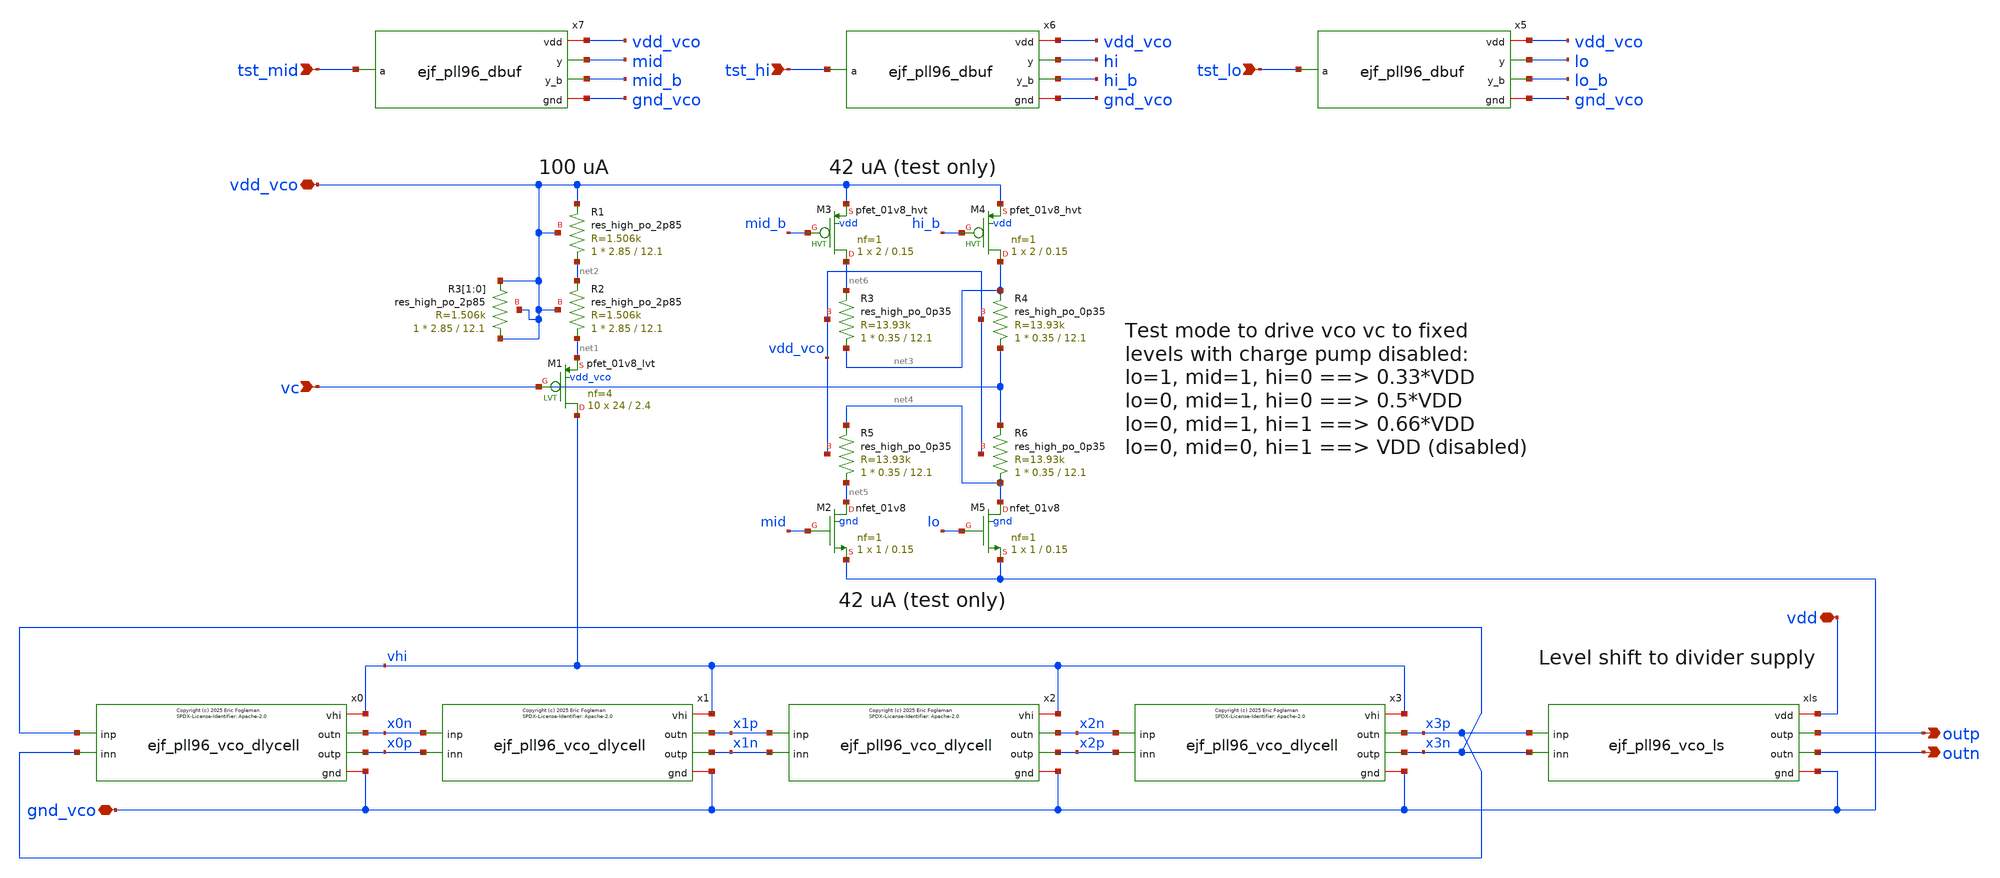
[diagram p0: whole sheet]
** sch_path: xschem/ejf_pll96_vco.sch
* xschem/ejf_pll96_vco_dlycell.sym:
* Copyright (c) 2025 Eric Fogleman
**.subckt ejf_pll96_vco vc vdd_vco outp gnd_vco vdd outn tst_mid tst_hi tst_lo
*.ipin vc
*.iopin vdd_vco
*.opin outp
*.iopin gnd_vco
*.iopin vdd
*.opin outn
*.ipin tst_mid
*.ipin tst_hi
*.ipin tst_lo
x1 vhi x1p x1n x0n x0p gnd_vco ejf_pll96_vco_dlycell
x2 vhi x2n x2p x1p x1n gnd_vco ejf_pll96_vco_dlycell
x0 vhi x0n x0p x3n x3p gnd_vco ejf_pll96_vco_dlycell
x3 vhi x3p x3n x2n x2p gnd_vco ejf_pll96_vco_dlycell
xls vdd x3p outp outn x3n gnd_vco ejf_pll96_vco_ls
XM1 vhi vc net1 vdd_vco sky130_fd_pr__pfet_01v8_lvt L=2.4 W=24 nf=4 ad='int((nf+1)/2) * W/nf * 0.29'
+ as='int((nf+2)/2) * W/nf * 0.29' pd='2*int((nf+1)/2) * (W/nf + 0.29)' ps='2*int((nf+2)/2) * (W/nf + 0.29)'
+ nrd='0.29 / W' nrs='0.29 / W' sa=0 sb=0 sd=0 mult=10 m=10
XR1 net2 vdd_vco vdd_vco sky130_fd_pr__res_high_po_2p85 L=12.1 mult=1 m=1
XR2 net1 net2 vdd_vco sky130_fd_pr__res_high_po_2p85 L=12.1 mult=1 m=1
XR3[1] vdd_vco vdd_vco vdd_vco sky130_fd_pr__res_high_po_2p85 L=12.1 mult=1 m=1
XR3[0] vdd_vco vdd_vco vdd_vco sky130_fd_pr__res_high_po_2p85 L=12.1 mult=1 m=1
XR3 net3 net6 vdd_vco sky130_fd_pr__res_high_po_0p35 L=12.1 mult=1 m=1
XR4 vc net3 vdd_vco sky130_fd_pr__res_high_po_0p35 L=12.1 mult=1 m=1
XR5 net5 net4 vdd_vco sky130_fd_pr__res_high_po_0p35 L=12.1 mult=1 m=1
XR6 net4 vc vdd_vco sky130_fd_pr__res_high_po_0p35 L=12.1 mult=1 m=1
XM2 net5 mid gnd_vco gnd sky130_fd_pr__nfet_01v8 L=0.15 W=1 nf=1 ad='int((nf+1)/2) * W/nf * 0.29' as='int((nf+2)/2) * W/nf * 0.29'
+ pd='2*int((nf+1)/2) * (W/nf + 0.29)' ps='2*int((nf+2)/2) * (W/nf + 0.29)' nrd='0.29 / W' nrs='0.29 / W'
+ sa=0 sb=0 sd=0 mult=1 m=1
XM3 net6 mid_b vdd_vco vdd sky130_fd_pr__pfet_01v8_hvt L=0.15 W=2 nf=1 ad='int((nf+1)/2) * W/nf * 0.29'
+ as='int((nf+2)/2) * W/nf * 0.29' pd='2*int((nf+1)/2) * (W/nf + 0.29)' ps='2*int((nf+2)/2) * (W/nf + 0.29)'
+ nrd='0.29 / W' nrs='0.29 / W' sa=0 sb=0 sd=0 mult=1 m=1
XM4 net3 hi_b vdd_vco vdd sky130_fd_pr__pfet_01v8_hvt L=0.15 W=2 nf=1 ad='int((nf+1)/2) * W/nf * 0.29'
+ as='int((nf+2)/2) * W/nf * 0.29' pd='2*int((nf+1)/2) * (W/nf + 0.29)' ps='2*int((nf+2)/2) * (W/nf + 0.29)'
+ nrd='0.29 / W' nrs='0.29 / W' sa=0 sb=0 sd=0 mult=1 m=1
XM5 net4 lo gnd_vco gnd sky130_fd_pr__nfet_01v8 L=0.15 W=1 nf=1 ad='int((nf+1)/2) * W/nf * 0.29' as='int((nf+2)/2) * W/nf * 0.29'
+ pd='2*int((nf+1)/2) * (W/nf + 0.29)' ps='2*int((nf+2)/2) * (W/nf + 0.29)' nrd='0.29 / W' nrs='0.29 / W'
+ sa=0 sb=0 sd=0 mult=1 m=1
x5 vdd_vco tst_lo lo lo_b gnd_vco ejf_pll96_dbuf
x6 vdd_vco tst_hi hi hi_b gnd_vco ejf_pll96_dbuf
x7 vdd_vco tst_mid mid mid_b gnd_vco ejf_pll96_dbuf
**.ends

* expanding   symbol:  ejf_pll96_vco_dlycell.sym # of pins=6
** sym_path: xschem/ejf_pll96_vco_dlycell.sym
** sch_path: xschem/ejf_pll96_vco_dlycell.sch
.subckt ejf_pll96_vco_dlycell vhi outn outp inp inn gnd
*.ipin inp
*.opin outn
*.ipin inn
*.opin outp
*.iopin vhi
*.iopin gnd
XM11 outp outn gnd gnd sky130_fd_pr__nfet_01v8 L=0.44 W=1.22 nf=1 ad='int((nf+1)/2) * W/nf * 0.29' as='int((nf+2)/2) * W/nf * 0.29'
+ pd='2*int((nf+1)/2) * (W/nf + 0.29)' ps='2*int((nf+2)/2) * (W/nf + 0.29)' nrd='0.29 / W' nrs='0.29 / W'
+ sa=0 sb=0 sd=0 mult=1 m=1
XM13 outn inp gnd gnd sky130_fd_pr__nfet_01v8 L=0.44 W=4.88 nf=4 ad='int((nf+1)/2) * W/nf * 0.29' as='int((nf+2)/2) * W/nf * 0.29'
+ pd='2*int((nf+1)/2) * (W/nf + 0.29)' ps='2*int((nf+2)/2) * (W/nf + 0.29)' nrd='0.29 / W' nrs='0.29 / W'
+ sa=0 sb=0 sd=0 mult=1 m=1
XM14 outn inp vhi vhi sky130_fd_pr__pfet_01v8_hvt L=0.44 W=19.44 nf=6 ad='int((nf+1)/2) * W/nf * 0.29'
+ as='int((nf+2)/2) * W/nf * 0.29' pd='2*int((nf+1)/2) * (W/nf + 0.29)' ps='2*int((nf+2)/2) * (W/nf + 0.29)'
+ nrd='0.29 / W' nrs='0.29 / W' sa=0 sb=0 sd=0 mult=1 m=1
XM27 outn outp gnd gnd sky130_fd_pr__nfet_01v8 L=0.44 W=1.22 nf=1 ad='int((nf+1)/2) * W/nf * 0.29' as='int((nf+2)/2) * W/nf * 0.29'
+ pd='2*int((nf+1)/2) * (W/nf + 0.29)' ps='2*int((nf+2)/2) * (W/nf + 0.29)' nrd='0.29 / W' nrs='0.29 / W'
+ sa=0 sb=0 sd=0 mult=1 m=1
XM31 outp inn gnd gnd sky130_fd_pr__nfet_01v8 L=0.44 W=4.88 nf=4 ad='int((nf+1)/2) * W/nf * 0.29' as='int((nf+2)/2) * W/nf * 0.29'
+ pd='2*int((nf+1)/2) * (W/nf + 0.29)' ps='2*int((nf+2)/2) * (W/nf + 0.29)' nrd='0.29 / W' nrs='0.29 / W'
+ sa=0 sb=0 sd=0 mult=1 m=1
XM30 outp inn vhi vhi sky130_fd_pr__pfet_01v8_hvt L=0.44 W=19.44 nf=6 ad='int((nf+1)/2) * W/nf * 0.29'
+ as='int((nf+2)/2) * W/nf * 0.29' pd='2*int((nf+1)/2) * (W/nf + 0.29)' ps='2*int((nf+2)/2) * (W/nf + 0.29)'
+ nrd='0.29 / W' nrs='0.29 / W' sa=0 sb=0 sd=0 mult=1 m=1
C3 inp gnd {CP} m=1
C4 inn gnd {CP} m=1
**** begin user architecture code

* Copyright (c) Eric Fogleman 2025
* SPDX-License-Identifier: Apache-2.0

**** end user architecture code
.ends


* expanding   symbol:  ejf_pll96_vco_ls.sym # of pins=6
** sym_path: xschem/ejf_pll96_vco_ls.sym
** sch_path: xschem/ejf_pll96_vco_ls.sch
.subckt ejf_pll96_vco_ls vdd inp outp outn inn gnd
*.ipin inp
*.opin outn
*.ipin inn
*.opin outp
*.iopin vdd
*.iopin gnd
XM5 net1 ls_outn vdd vdd sky130_fd_pr__pfet_01v8_hvt L=0.15 W=2 nf=1 ad='int((nf+1)/2) * W/nf * 0.29'
+ as='int((nf+2)/2) * W/nf * 0.29' pd='2*int((nf+1)/2) * (W/nf + 0.29)' ps='2*int((nf+2)/2) * (W/nf + 0.29)'
+ nrd='0.29 / W' nrs='0.29 / W' sa=0 sb=0 sd=0 mult=1 m=1
XM1 ls_outn inp gnd gnd sky130_fd_pr__nfet_01v8 L=0.15 W=2 nf=1 ad='int((nf+1)/2) * W/nf * 0.29' as='int((nf+2)/2) * W/nf * 0.29'
+ pd='2*int((nf+1)/2) * (W/nf + 0.29)' ps='2*int((nf+2)/2) * (W/nf + 0.29)' nrd='0.29 / W' nrs='0.29 / W'
+ sa=0 sb=0 sd=0 mult=1 m=1
XM2 ls_outp inn gnd gnd sky130_fd_pr__nfet_01v8 L=0.15 W=2 nf=1 ad='int((nf+1)/2) * W/nf * 0.29' as='int((nf+2)/2) * W/nf * 0.29'
+ pd='2*int((nf+1)/2) * (W/nf + 0.29)' ps='2*int((nf+2)/2) * (W/nf + 0.29)' nrd='0.29 / W' nrs='0.29 / W'
+ sa=0 sb=0 sd=0 mult=1 m=1
XM3 net2 ls_outp vdd vdd sky130_fd_pr__pfet_01v8_hvt L=0.15 W=2 nf=1 ad='int((nf+1)/2) * W/nf * 0.29'
+ as='int((nf+2)/2) * W/nf * 0.29' pd='2*int((nf+1)/2) * (W/nf + 0.29)' ps='2*int((nf+2)/2) * (W/nf + 0.29)'
+ nrd='0.29 / W' nrs='0.29 / W' sa=0 sb=0 sd=0 mult=1 m=1
XM4 ls_outn inp net2 vdd sky130_fd_pr__pfet_01v8_hvt L=0.15 W=2 nf=1 ad='int((nf+1)/2) * W/nf * 0.29'
+ as='int((nf+2)/2) * W/nf * 0.29' pd='2*int((nf+1)/2) * (W/nf + 0.29)' ps='2*int((nf+2)/2) * (W/nf + 0.29)'
+ nrd='0.29 / W' nrs='0.29 / W' sa=0 sb=0 sd=0 mult=1 m=1
XM6 ls_outp inn net1 vdd sky130_fd_pr__pfet_01v8_hvt L=0.15 W=2 nf=1 ad='int((nf+1)/2) * W/nf * 0.29'
+ as='int((nf+2)/2) * W/nf * 0.29' pd='2*int((nf+1)/2) * (W/nf + 0.29)' ps='2*int((nf+2)/2) * (W/nf + 0.29)'
+ nrd='0.29 / W' nrs='0.29 / W' sa=0 sb=0 sd=0 mult=1 m=1
XM7 outn ls_outp gnd gnd sky130_fd_pr__nfet_01v8 L=0.15 W=2 nf=1 ad='int((nf+1)/2) * W/nf * 0.29' as='int((nf+2)/2) * W/nf * 0.29'
+ pd='2*int((nf+1)/2) * (W/nf + 0.29)' ps='2*int((nf+2)/2) * (W/nf + 0.29)' nrd='0.29 / W' nrs='0.29 / W'
+ sa=0 sb=0 sd=0 mult=1 m=1
XM8 outn ls_outp vdd vdd sky130_fd_pr__pfet_01v8_hvt L=0.15 W=4 nf=1 ad='int((nf+1)/2) * W/nf * 0.29'
+ as='int((nf+2)/2) * W/nf * 0.29' pd='2*int((nf+1)/2) * (W/nf + 0.29)' ps='2*int((nf+2)/2) * (W/nf + 0.29)'
+ nrd='0.29 / W' nrs='0.29 / W' sa=0 sb=0 sd=0 mult=1 m=1
XM9 outp ls_outn gnd gnd sky130_fd_pr__nfet_01v8 L=0.15 W=2 nf=1 ad='int((nf+1)/2) * W/nf * 0.29' as='int((nf+2)/2) * W/nf * 0.29'
+ pd='2*int((nf+1)/2) * (W/nf + 0.29)' ps='2*int((nf+2)/2) * (W/nf + 0.29)' nrd='0.29 / W' nrs='0.29 / W'
+ sa=0 sb=0 sd=0 mult=1 m=1
XM10 outp ls_outn vdd vdd sky130_fd_pr__pfet_01v8_hvt L=0.15 W=4 nf=1 ad='int((nf+1)/2) * W/nf * 0.29'
+ as='int((nf+2)/2) * W/nf * 0.29' pd='2*int((nf+1)/2) * (W/nf + 0.29)' ps='2*int((nf+2)/2) * (W/nf + 0.29)'
+ nrd='0.29 / W' nrs='0.29 / W' sa=0 sb=0 sd=0 mult=1 m=1
.ends


* expanding   symbol:  ejf_pll96_dbuf.sym # of pins=5
** sym_path: xschem/ejf_pll96_dbuf.sym
** sch_path: xschem/ejf_pll96_dbuf.sch
.subckt ejf_pll96_dbuf vdd a y y_b gnd
*.ipin a
*.iopin vdd
*.iopin gnd
*.opin y
*.opin y_b
XMP1 y_b a vdd vdd sky130_fd_pr__pfet_01v8_hvt L=0.15 W=2 nf=1 ad='int((nf+1)/2) * W/nf * 0.29' as='int((nf+2)/2) * W/nf * 0.29'
+ pd='2*int((nf+1)/2) * (W/nf + 0.29)' ps='2*int((nf+2)/2) * (W/nf + 0.29)' nrd='0.29 / W' nrs='0.29 / W'
+ sa=0 sb=0 sd=0 mult=1 m=1
XMP3 y y_b vdd vdd sky130_fd_pr__pfet_01v8_hvt L=0.15 W=2 nf=1 ad='int((nf+1)/2) * W/nf * 0.29' as='int((nf+2)/2) * W/nf * 0.29'
+ pd='2*int((nf+1)/2) * (W/nf + 0.29)' ps='2*int((nf+2)/2) * (W/nf + 0.29)' nrd='0.29 / W' nrs='0.29 / W'
+ sa=0 sb=0 sd=0 mult=1 m=1
XMN4 y y_b gnd gnd sky130_fd_pr__nfet_01v8 L=0.15 W=1 nf=1 ad='int((nf+1)/2) * W/nf * 0.29' as='int((nf+2)/2) * W/nf * 0.29'
+ pd='2*int((nf+1)/2) * (W/nf + 0.29)' ps='2*int((nf+2)/2) * (W/nf + 0.29)' nrd='0.29 / W' nrs='0.29 / W'
+ sa=0 sb=0 sd=0 mult=1 m=1
XMN2 y_b a gnd gnd sky130_fd_pr__nfet_01v8 L=0.15 W=1 nf=1 ad='int((nf+1)/2) * W/nf * 0.29' as='int((nf+2)/2) * W/nf * 0.29'
+ pd='2*int((nf+1)/2) * (W/nf + 0.29)' ps='2*int((nf+2)/2) * (W/nf + 0.29)' nrd='0.29 / W' nrs='0.29 / W'
+ sa=0 sb=0 sd=0 mult=1 m=1
.ends

.end
